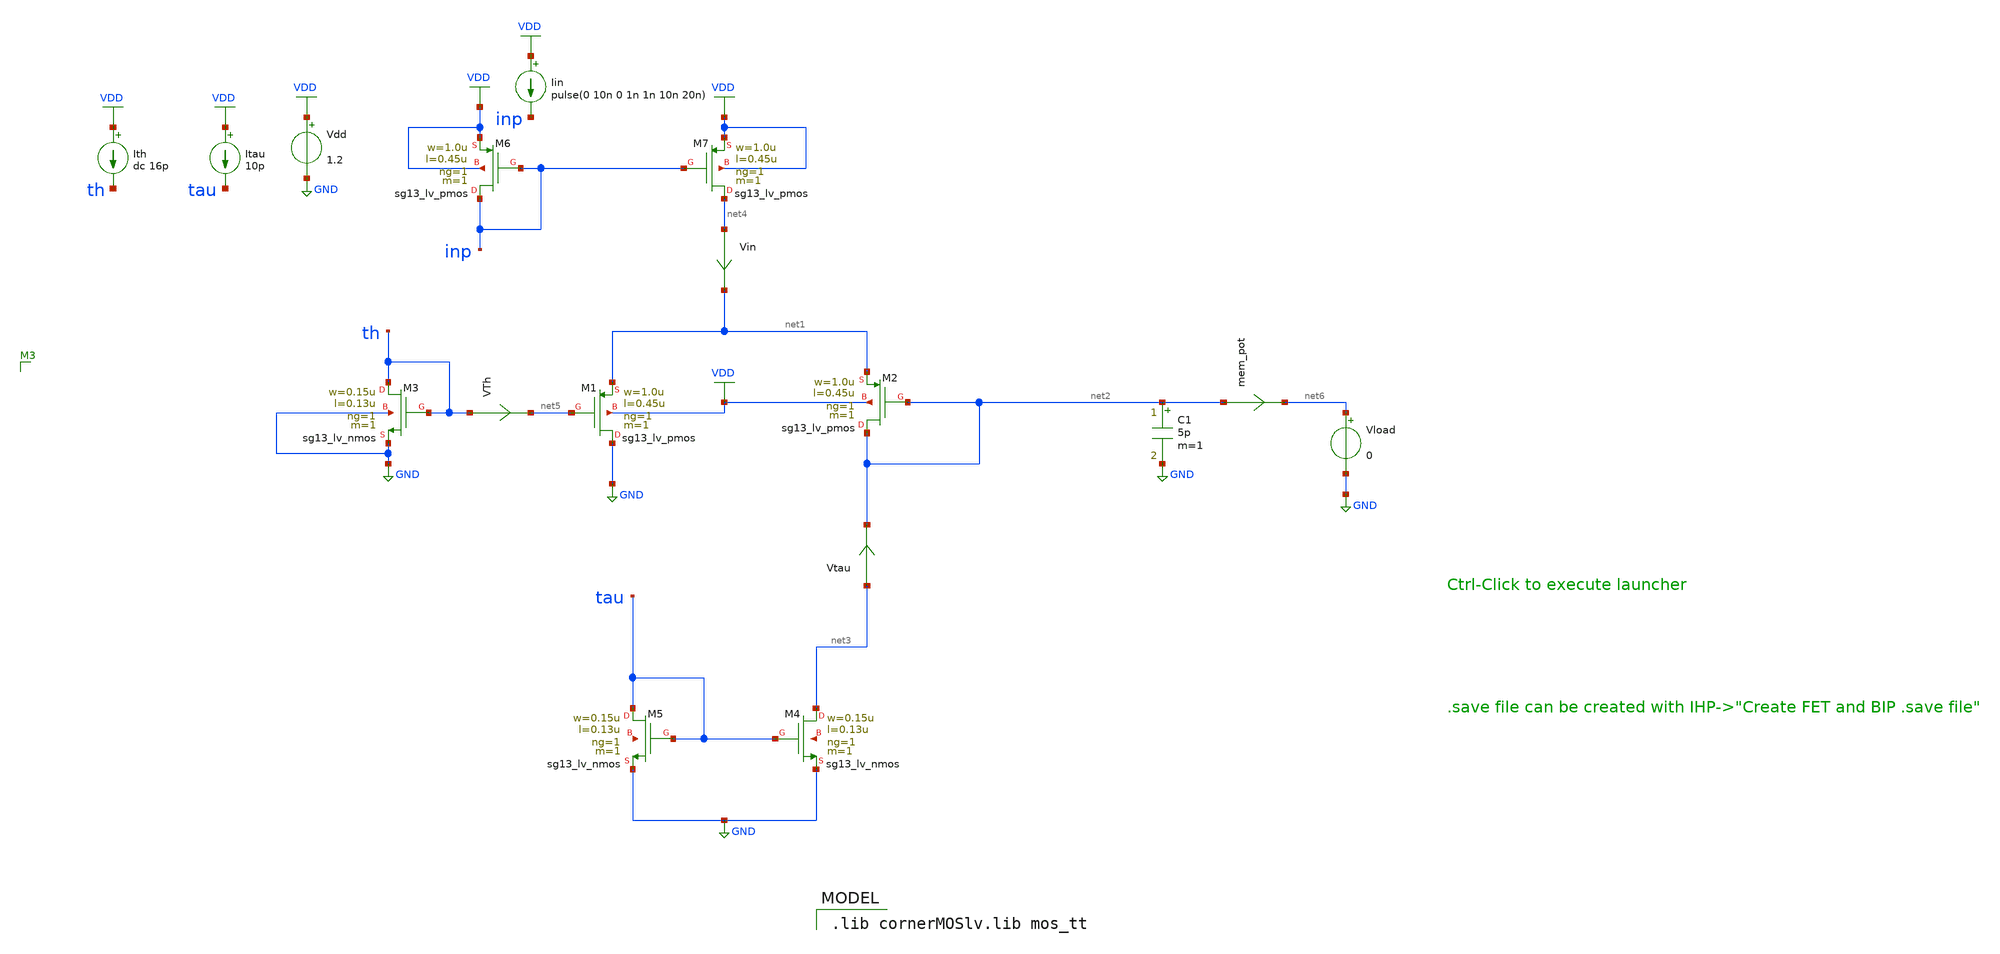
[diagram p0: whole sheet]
** sch_path: blocks/composite/dpi_adexp_neuron/design_data/xschem/legacy/DPI_try_1.sch
* Copyright 2023 IHP PDK Authors
**.subckt DPI_try_1
Vload net6 GND 0
mem_pot net2 net6 0
.save i(mem_pot)
XM1 GND net5 net1 VDD sg13_lv_pmos w=1.0u l=0.45u ng=1 m=1 mm_ok=1
XM2 net2 net2 net1 VDD sg13_lv_pmos w=1.0u l=0.45u ng=1 m=1 mm_ok=1
XM4 net3 tau GND net7 sg13_lv_nmos w=0.15u l=0.13u ng=1 m=1 mm_ok=1
XM5 tau tau GND net8 sg13_lv_nmos w=0.15u l=0.13u ng=1 m=1 mm_ok=1
XM6 inp inp VDD VDD sg13_lv_pmos w=1.0u l=0.45u ng=1 m=1 mm_ok=1
XM7 net4 inp VDD VDD sg13_lv_pmos w=1.0u l=0.45u ng=1 m=1 mm_ok=1
Vin net4 net1 0
.save i(vin)
Vtau net3 net2 0
.save i(vtau)
XM3 th th GND GND sg13_lv_nmos w=0.15u l=0.13u ng=1 m=1 mm_ok=1
VTh th net5 0
.save i(vth)
C1 net2 GND 5p m=1
Vdd VDD GND 1.2
Iin VDD inp pulse(0 10n 0 1n 1n 10n 20n)
Ith VDD th dc 16p
Itau VDD tau 10p
**** begin user architecture code


.options savecurrrents
.include DPI_try_1.save
.param temp=27
.control
save all
op
write DPI_try_1.raw
set appendwrite
*dc Vds 0 1.2 0.01 Vgs 0.3 1.0 0.1
*dc Vgs 0 0.5 0.05
dc vds 0 -1.2 -0.01 Vgs -0.35 -1.1 -0.05
write DPI_try_1.raw
.endc


 .lib cornerMOSlv.lib mos_tt

**** end user architecture code
**.ends
.GLOBAL GND
.GLOBAL VDD
.end
